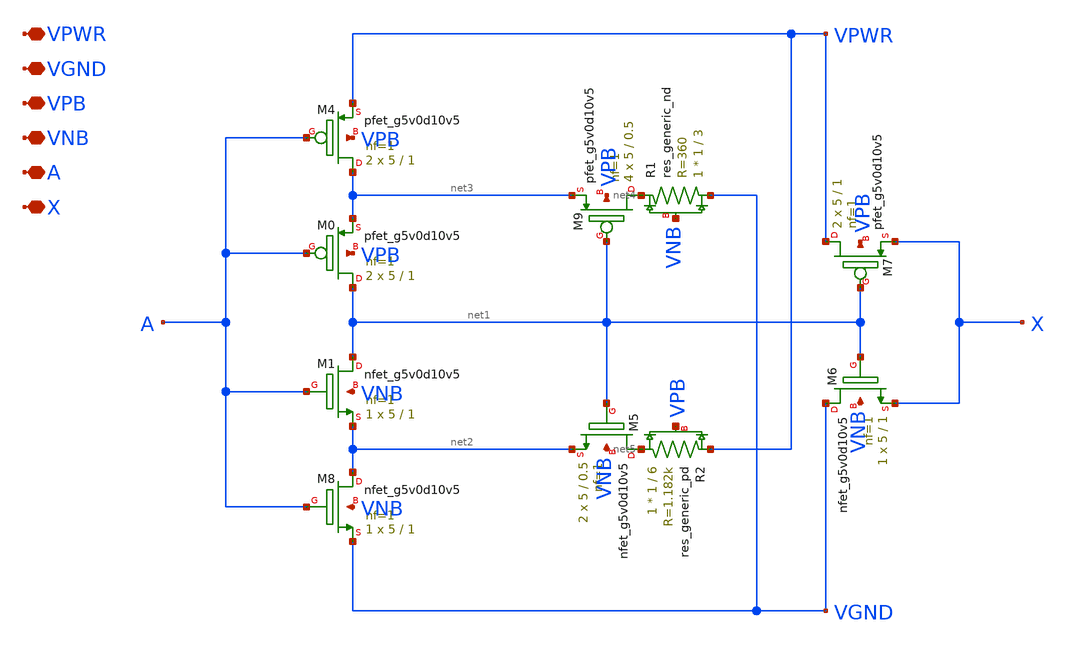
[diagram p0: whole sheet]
** sch_path: design/oscillator/schmittbuf.sch
**.subckt schmittbuf VPWR VGND VPB VNB A X
*.iopin VPWR
*.iopin VGND
*.iopin VPB
*.iopin VNB
*.iopin A
*.iopin X
XM1 net1 A net2 VNB sky130_fd_pr__nfet_g5v0d10v5 L=1 W=5 nf=1 ad='int((nf+1)/2) * W/nf * 0.29' as='int((nf+2)/2) * W/nf * 0.29'
+ pd='2*int((nf+1)/2) * (W/nf + 0.29)' ps='2*int((nf+2)/2) * (W/nf + 0.29)' nrd='0.29 / W' nrs='0.29 / W'
+ sa=0 sb=0 sd=0 mult=1 m=1
XM8 net2 A VGND VNB sky130_fd_pr__nfet_g5v0d10v5 L=1 W=5 nf=1 ad='int((nf+1)/2) * W/nf * 0.29' as='int((nf+2)/2) * W/nf * 0.29'
+ pd='2*int((nf+1)/2) * (W/nf + 0.29)' ps='2*int((nf+2)/2) * (W/nf + 0.29)' nrd='0.29 / W' nrs='0.29 / W'
+ sa=0 sb=0 sd=0 mult=1 m=1
XM0 net1 A net3 VPB sky130_fd_pr__pfet_g5v0d10v5 L=1 W=5 nf=1 ad='int((nf+1)/2) * W/nf * 0.29' as='int((nf+2)/2) * W/nf * 0.29'
+ pd='2*int((nf+1)/2) * (W/nf + 0.29)' ps='2*int((nf+2)/2) * (W/nf + 0.29)' nrd='0.29 / W' nrs='0.29 / W'
+ sa=0 sb=0 sd=0 mult=2 m=2
XM4 net3 A VPWR VPB sky130_fd_pr__pfet_g5v0d10v5 L=1 W=5 nf=1 ad='int((nf+1)/2) * W/nf * 0.29' as='int((nf+2)/2) * W/nf * 0.29'
+ pd='2*int((nf+1)/2) * (W/nf + 0.29)' ps='2*int((nf+2)/2) * (W/nf + 0.29)' nrd='0.29 / W' nrs='0.29 / W'
+ sa=0 sb=0 sd=0 mult=2 m=2
XM7 VPWR net1 X VPB sky130_fd_pr__pfet_g5v0d10v5 L=1 W=5 nf=1 ad='int((nf+1)/2) * W/nf * 0.29' as='int((nf+2)/2) * W/nf * 0.29'
+ pd='2*int((nf+1)/2) * (W/nf + 0.29)' ps='2*int((nf+2)/2) * (W/nf + 0.29)' nrd='0.29 / W' nrs='0.29 / W'
+ sa=0 sb=0 sd=0 mult=2 m=2
XM6 VGND net1 X VNB sky130_fd_pr__nfet_g5v0d10v5 L=1 W=5 nf=1 ad='int((nf+1)/2) * W/nf * 0.29' as='int((nf+2)/2) * W/nf * 0.29'
+ pd='2*int((nf+1)/2) * (W/nf + 0.29)' ps='2*int((nf+2)/2) * (W/nf + 0.29)' nrd='0.29 / W' nrs='0.29 / W'
+ sa=0 sb=0 sd=0 mult=1 m=1
XM9 net4 net1 net3 VPB sky130_fd_pr__pfet_g5v0d10v5 L=0.5 W=5 nf=1 ad='int((nf+1)/2) * W/nf * 0.29' as='int((nf+2)/2) * W/nf * 0.29'
+ pd='2*int((nf+1)/2) * (W/nf + 0.29)' ps='2*int((nf+2)/2) * (W/nf + 0.29)' nrd='0.29 / W' nrs='0.29 / W'
+ sa=0 sb=0 sd=0 mult=4 m=4
XM5 net5 net1 net2 VNB sky130_fd_pr__nfet_g5v0d10v5 L=0.5 W=5 nf=1 ad='int((nf+1)/2) * W/nf * 0.29' as='int((nf+2)/2) * W/nf * 0.29'
+ pd='2*int((nf+1)/2) * (W/nf + 0.29)' ps='2*int((nf+2)/2) * (W/nf + 0.29)' nrd='0.29 / W' nrs='0.29 / W'
+ sa=0 sb=0 sd=0 mult=2 m=2
XR1 VGND net4 VNB sky130_fd_pr__res_generic_nd W=1 L=3 mult=1 m=1
XR2 net5 VPWR VPB sky130_fd_pr__res_generic_pd W=1 L=6 mult=1 m=1
**.ends
.end
